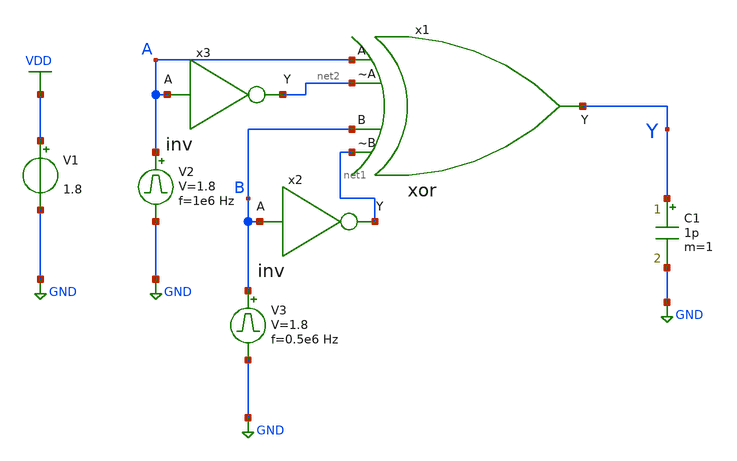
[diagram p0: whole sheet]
** sch_path: xschem/xor_tb.sch
**.subckt xor_tb
V1 VDD GND 1.8
V2 A GND pulse 0 1.8 '0.495/ 1e6 ' '0.01/1e6 ' '0.01/1e6 ' '0.49/1e6 ' '1/1e6 '
C1 Y GND 1p m=1
V3 B GND pulse 0 1.8 '0.495/ 0.5e6 ' '0.01/0.5e6 ' '0.01/0.5e6 ' '0.49/0.5e6 ' '1/0.5e6 '
x1 B Y A net2 net1 xor
x2 net1 B inv
x3 net2 A inv
**** begin user architecture code


.control
save all
tran 1n 2u
plot V(A) V(B)+2 V(Y)+4
.endc



** opencircuitdesign pdks install
.lib $::SKYWATER_MODELS/sky130.lib.spice tt


**** end user architecture code
**.ends
.GLOBAL VDD
.GLOBAL GND
.end
